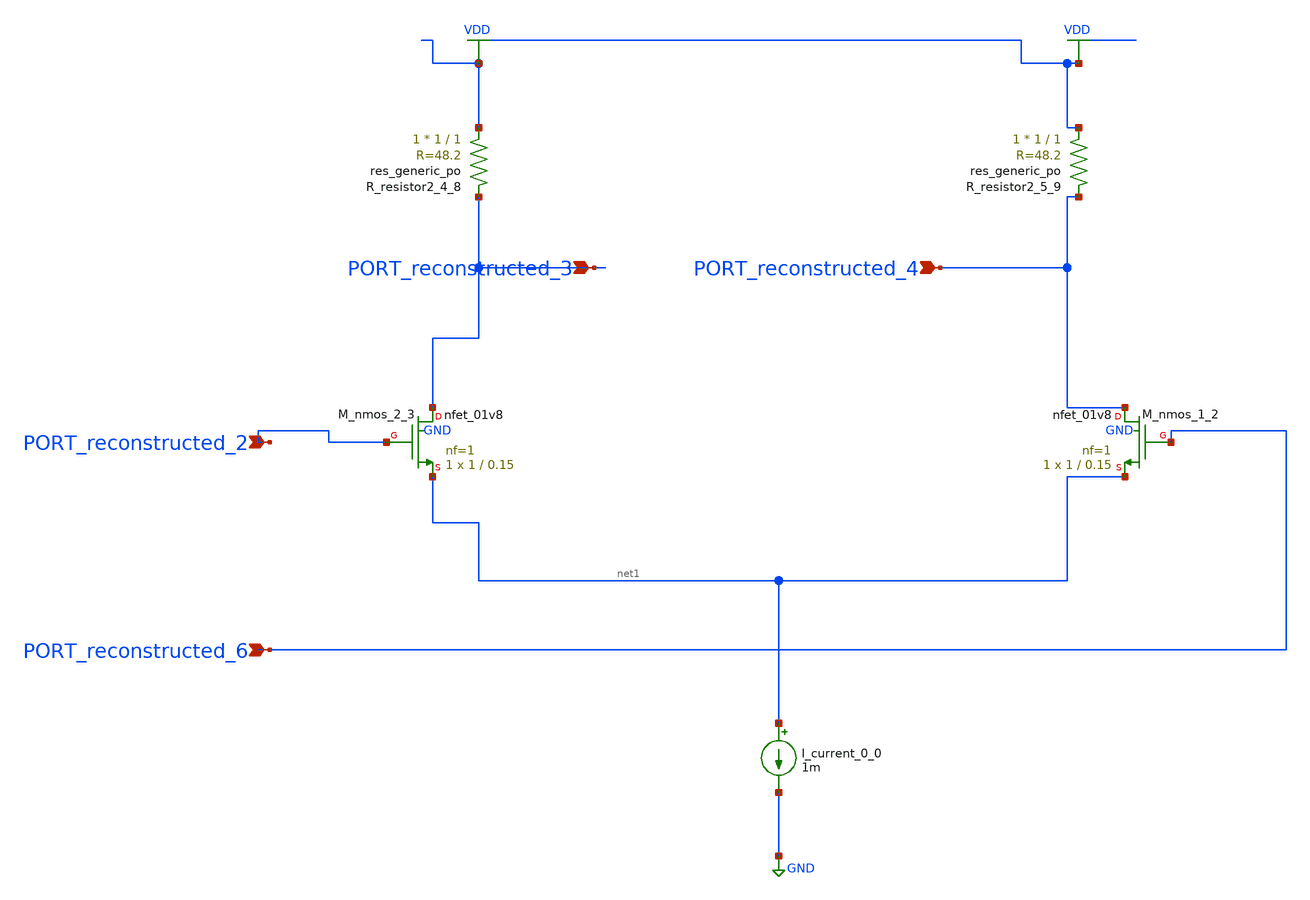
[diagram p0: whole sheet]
** sch_path: schematics/AMSNet/655.sch
**.subckt 655 PORT_reconstructed_6 PORT_reconstructed_2 PORT_reconstructed_3 PORT_reconstructed_4
*.ipin PORT_reconstructed_6
*.ipin PORT_reconstructed_2
*.ipin PORT_reconstructed_3
*.ipin PORT_reconstructed_4
I_current_0_0 net1 GND 1m
XM_nmos_1_2 PORT_reconstructed_4 PORT_reconstructed_6 net1 GND sky130_fd_pr__nfet_01v8 L=0.15 W=1 nf=1
+ ad='int((1 + 1)/2) * 1 / 1 * 0.29' as='int((1 + 2)/2) * 1 / 1 * 0.29' pd='2*int((1 + 1)/2) * (1 / 1 + 0.29)'
+ ps='2*int((1 + 2)/2) * (1 / 1 + 0.29)' nrd='0.29 / 1 ' nrs='0.29 / 1 ' sa=0 sb=0 sd=0 mult=1 m=1
XM_nmos_2_3 PORT_reconstructed_3 PORT_reconstructed_2 net1 GND sky130_fd_pr__nfet_01v8 L=0.15 W=1 nf=1
+ ad='int((1 + 1)/2) * 1 / 1 * 0.29' as='int((1 + 2)/2) * 1 / 1 * 0.29' pd='2*int((1 + 1)/2) * (1 / 1 + 0.29)'
+ ps='2*int((1 + 2)/2) * (1 / 1 + 0.29)' nrd='0.29 / 1 ' nrs='0.29 / 1 ' sa=0 sb=0 sd=0 mult=1 m=1
XR_resistor2_4_8 VDD PORT_reconstructed_3 sky130_fd_pr__res_generic_po W=1 L=1 m=1
XR_resistor2_5_9 VDD PORT_reconstructed_4 sky130_fd_pr__res_generic_po W=1 L=1 m=1
**.ends
.GLOBAL GND
.GLOBAL VDD
.end
